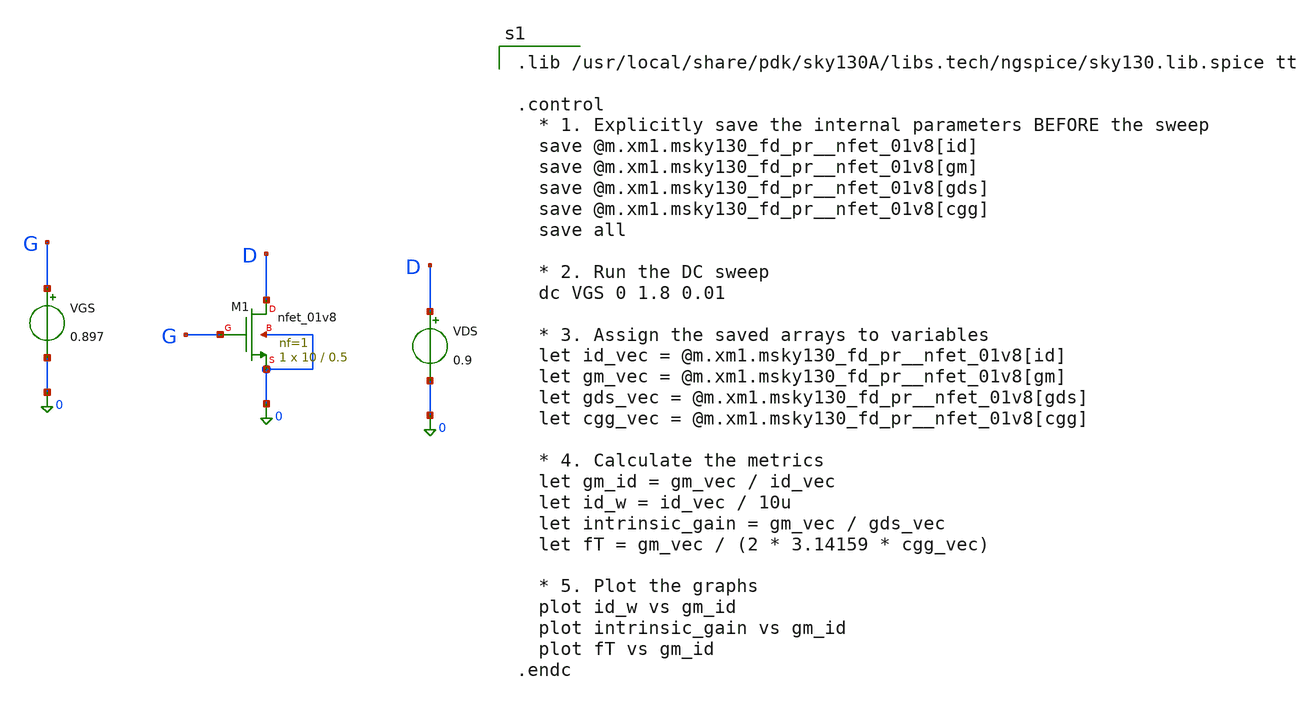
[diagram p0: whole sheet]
** sch_path: schematics/nmos.sch
**.subckt nmos
XM1 D G 0 0 sky130_fd_pr__nfet_01v8 L=0.5 W=10 nf=1 ad='int((1 + 1)/2) * 10 / 1 * 0.29' as='int((1 + 2)/2) * 10 / 1 * 0.29'
+ pd='2*int((1 + 1)/2) * (10 / 1 + 0.29)' ps='2*int((1 + 2)/2) * (10 / 1 + 0.29)' nrd='0.29 / 10 ' nrs='0.29 / 10 '
+ sa=0 sb=0 sd=0 mult=1 m=1
VGS G 0 0.897
VDS D 0 0.9
**** begin user architecture code

.lib /usr/local/share/pdk/sky130A/libs.tech/ngspice/sky130.lib.spice tt

.control
  * 1. Explicitly save the internal parameters BEFORE the sweep
  save @m.xm1.msky130_fd_pr__nfet_01v8[id]
  save @m.xm1.msky130_fd_pr__nfet_01v8[gm]
  save @m.xm1.msky130_fd_pr__nfet_01v8[gds]
  save @m.xm1.msky130_fd_pr__nfet_01v8[cgg]
  save all

  * 2. Run the DC sweep
  dc VGS 0 1.8 0.01

  * 3. Assign the saved arrays to variables
  let id_vec = @m.xm1.msky130_fd_pr__nfet_01v8[id]
  let gm_vec = @m.xm1.msky130_fd_pr__nfet_01v8[gm]
  let gds_vec = @m.xm1.msky130_fd_pr__nfet_01v8[gds]
  let cgg_vec = @m.xm1.msky130_fd_pr__nfet_01v8[cgg]

  * 4. Calculate the metrics
  let gm_id = gm_vec / id_vec
  let id_w = id_vec / 10u
  let intrinsic_gain = gm_vec / gds_vec
  let fT = gm_vec / (2 * 3.14159 * cgg_vec)

  * 5. Plot the graphs
  plot id_w vs gm_id
  plot intrinsic_gain vs gm_id
  plot fT vs gm_id
.endc

**** end user architecture code
**.ends
.end
